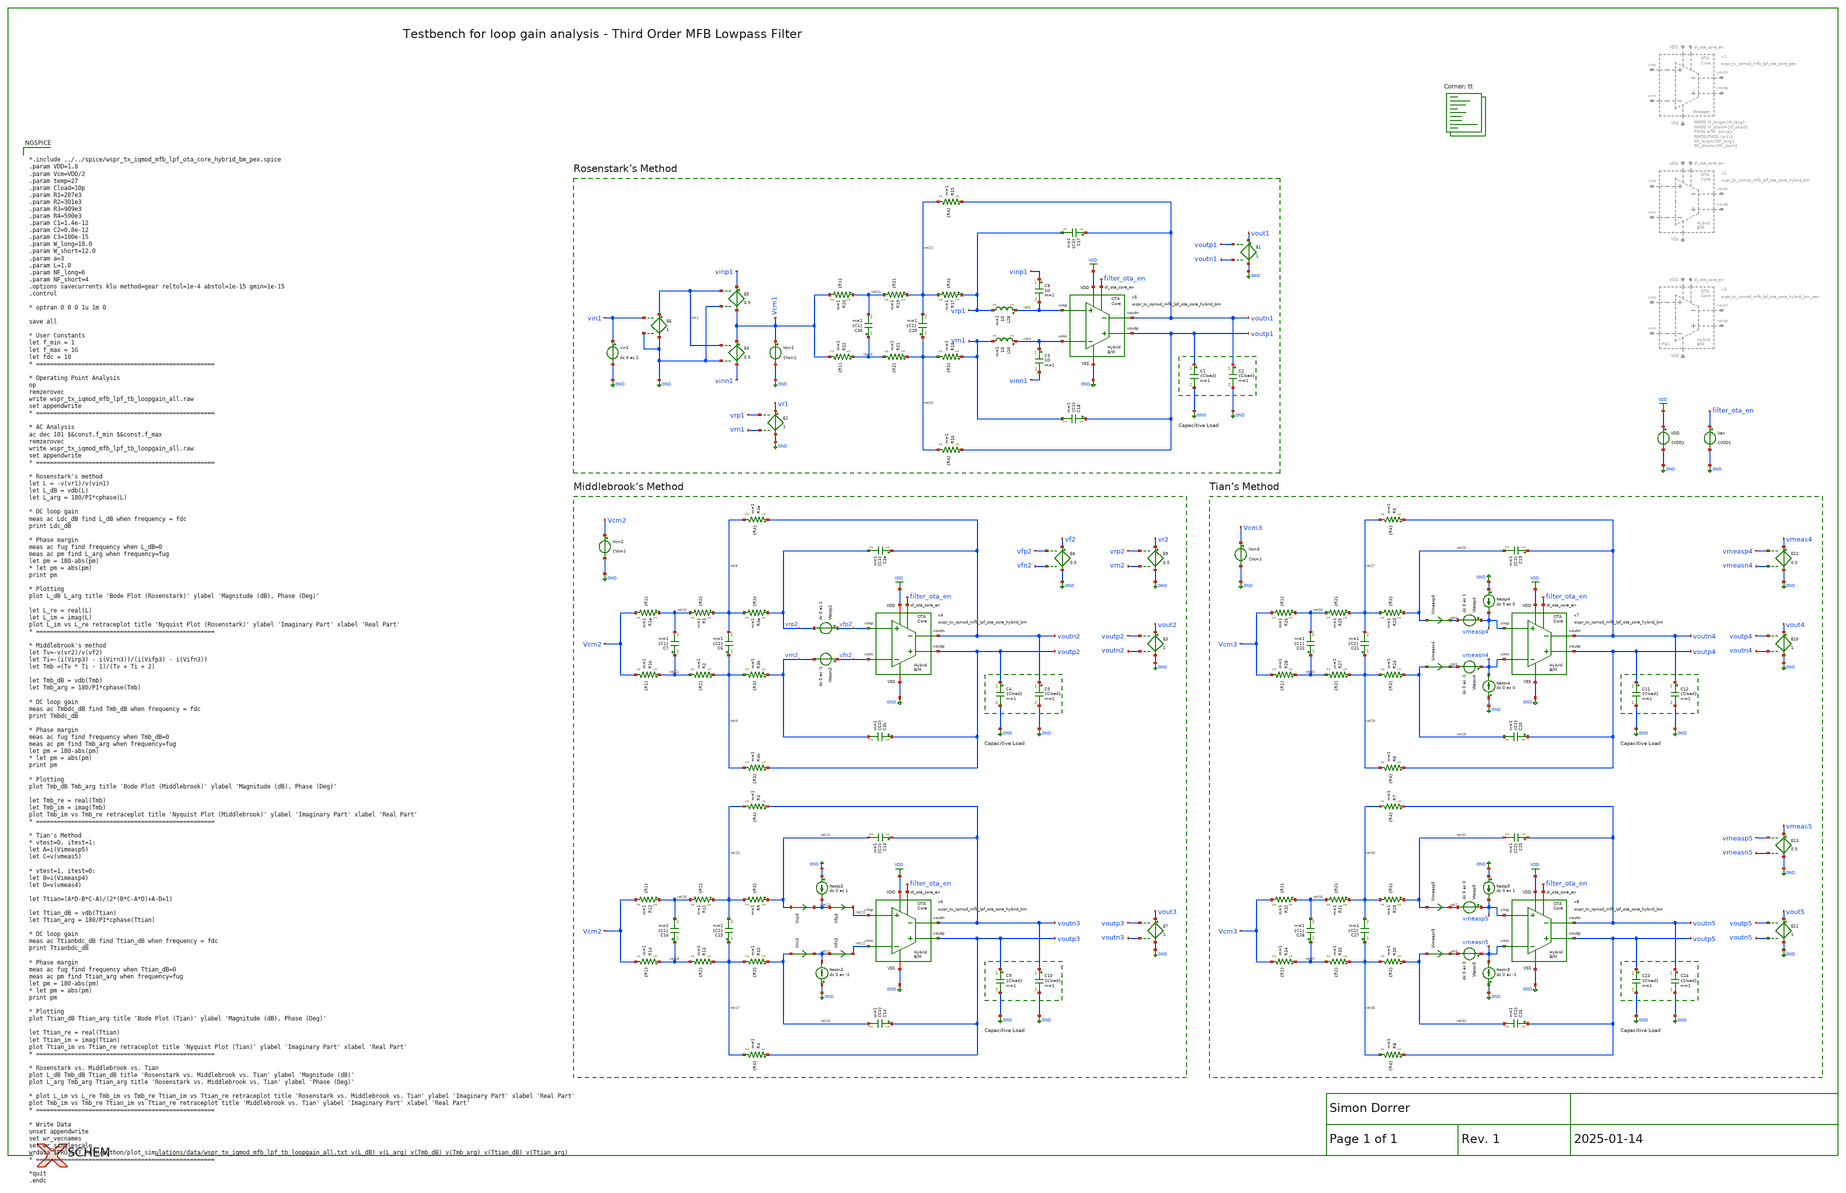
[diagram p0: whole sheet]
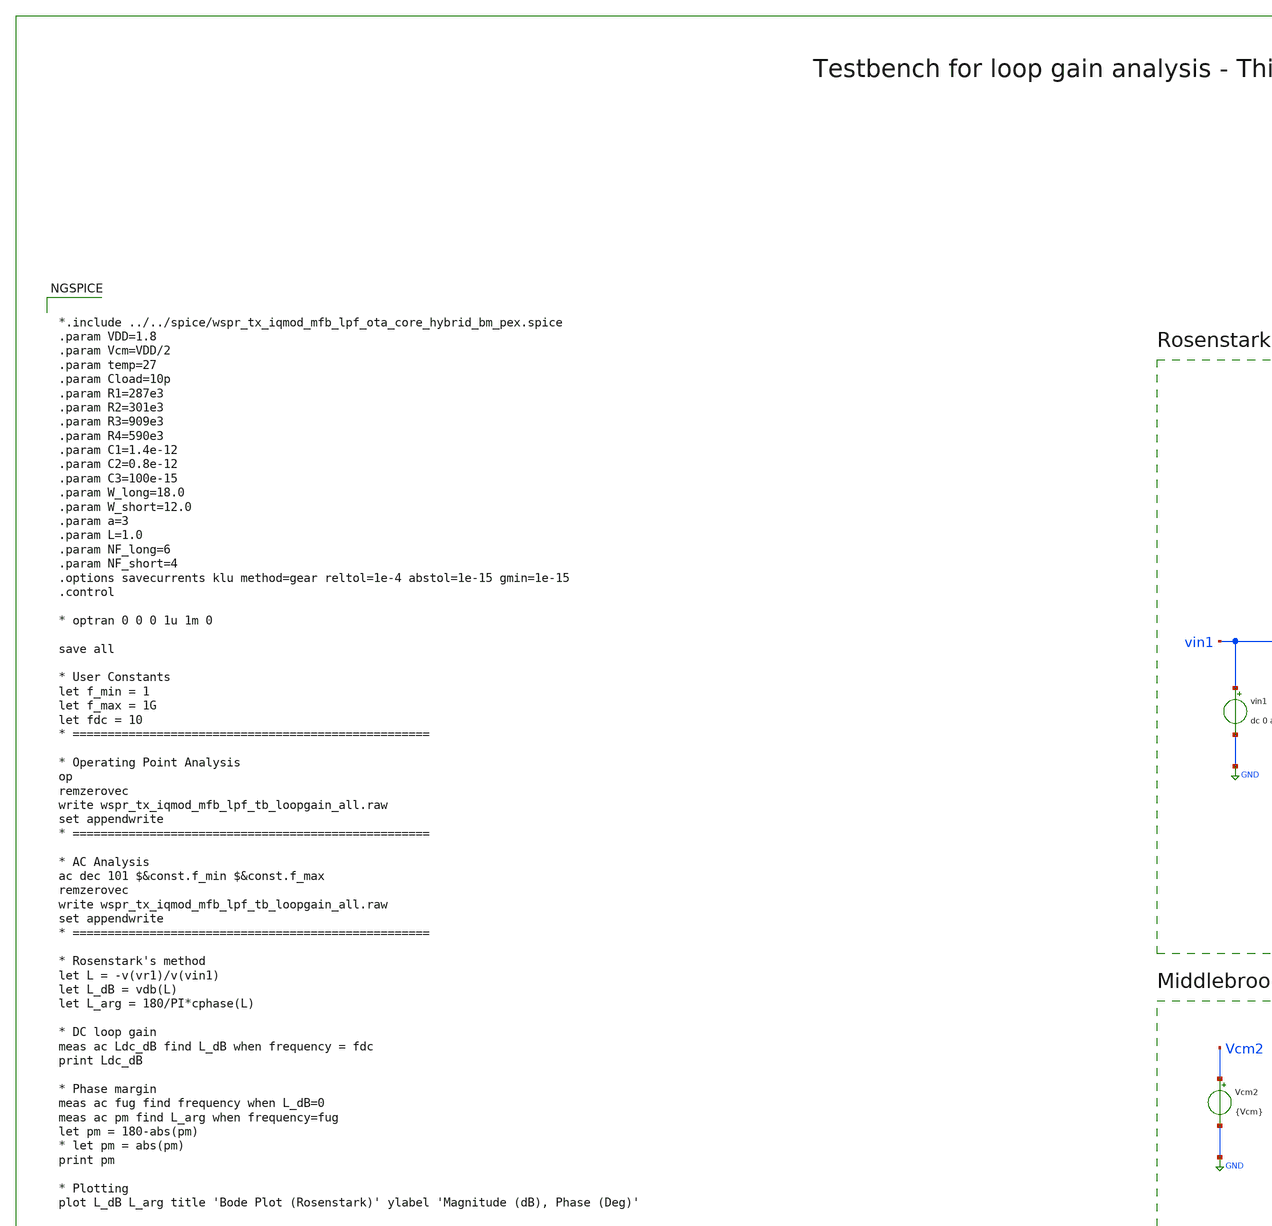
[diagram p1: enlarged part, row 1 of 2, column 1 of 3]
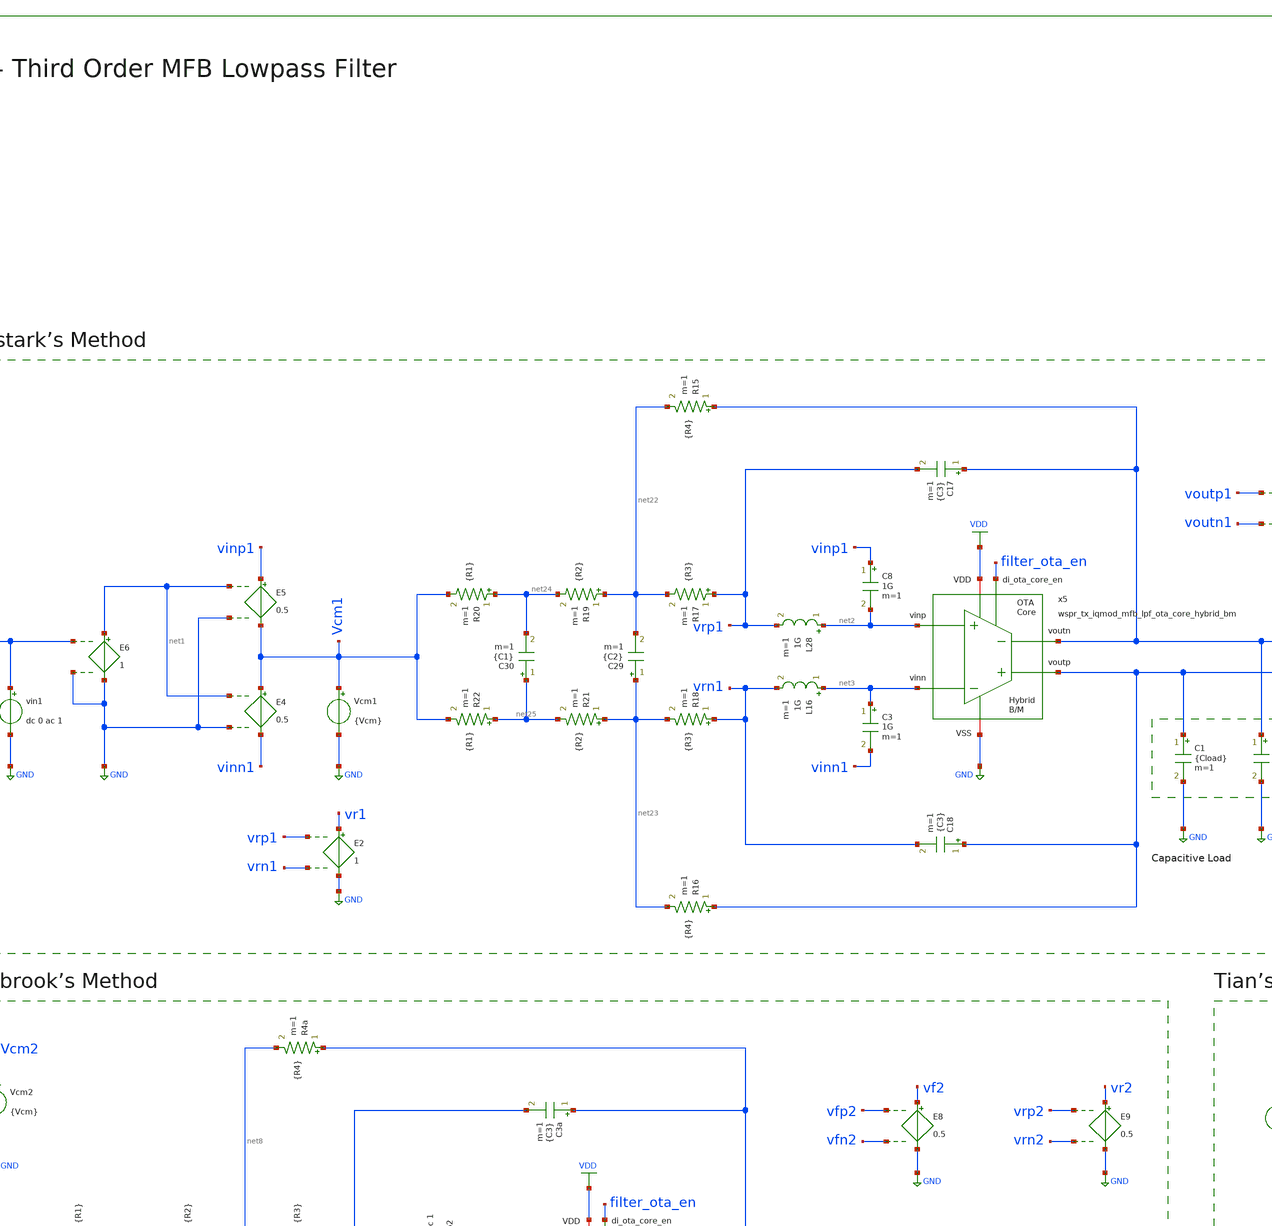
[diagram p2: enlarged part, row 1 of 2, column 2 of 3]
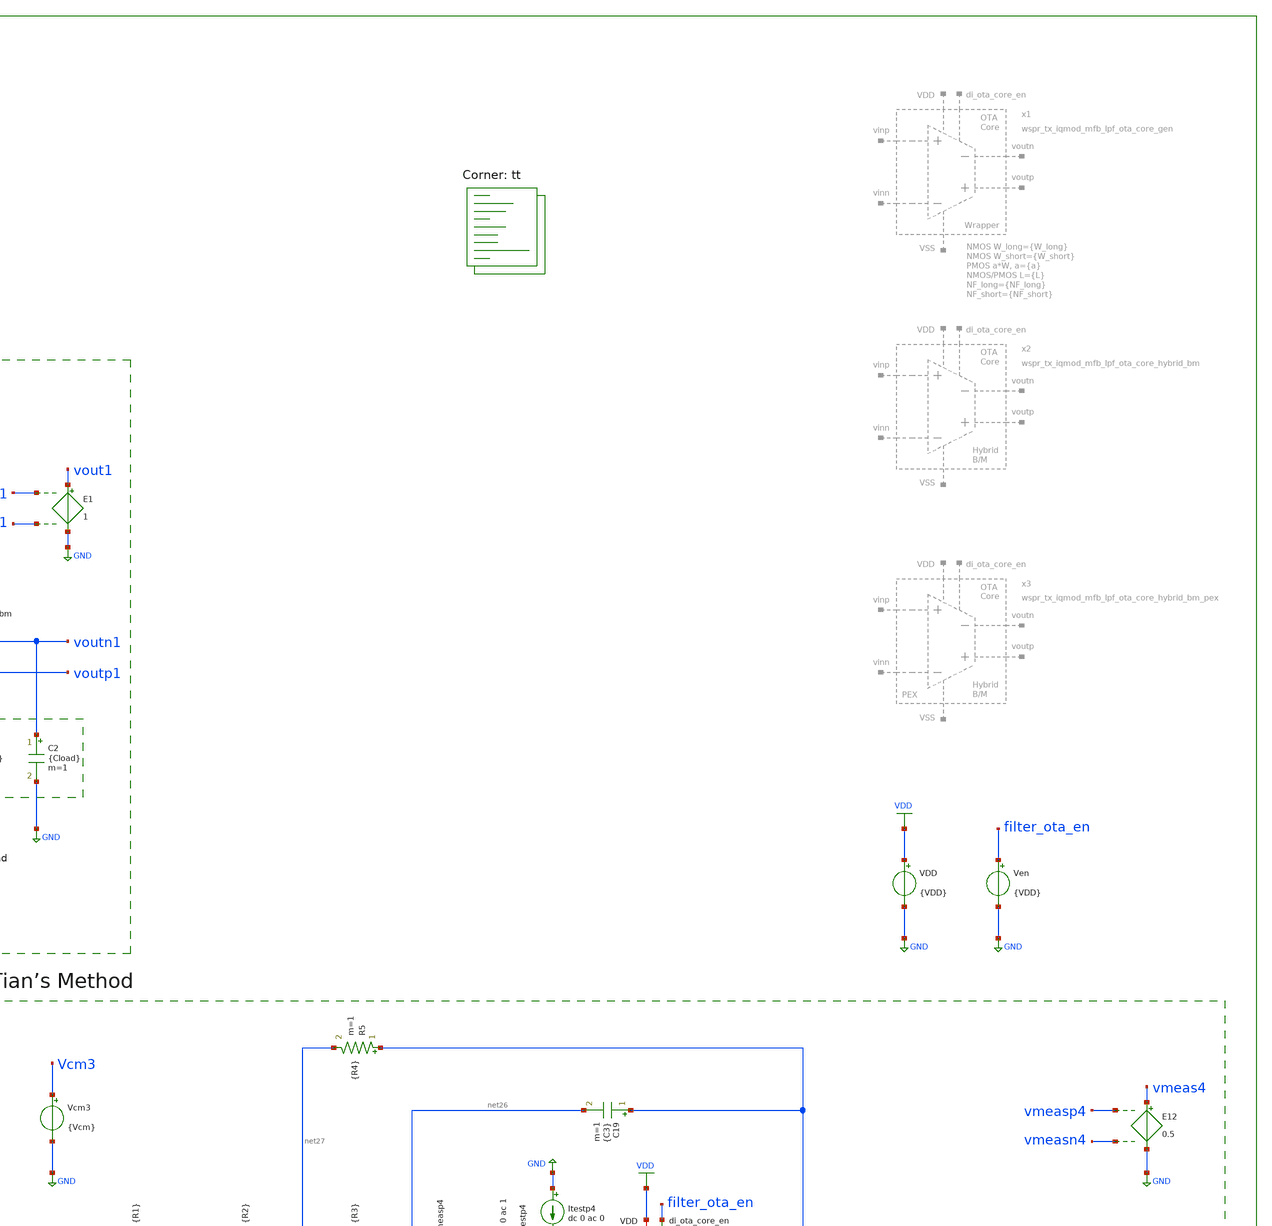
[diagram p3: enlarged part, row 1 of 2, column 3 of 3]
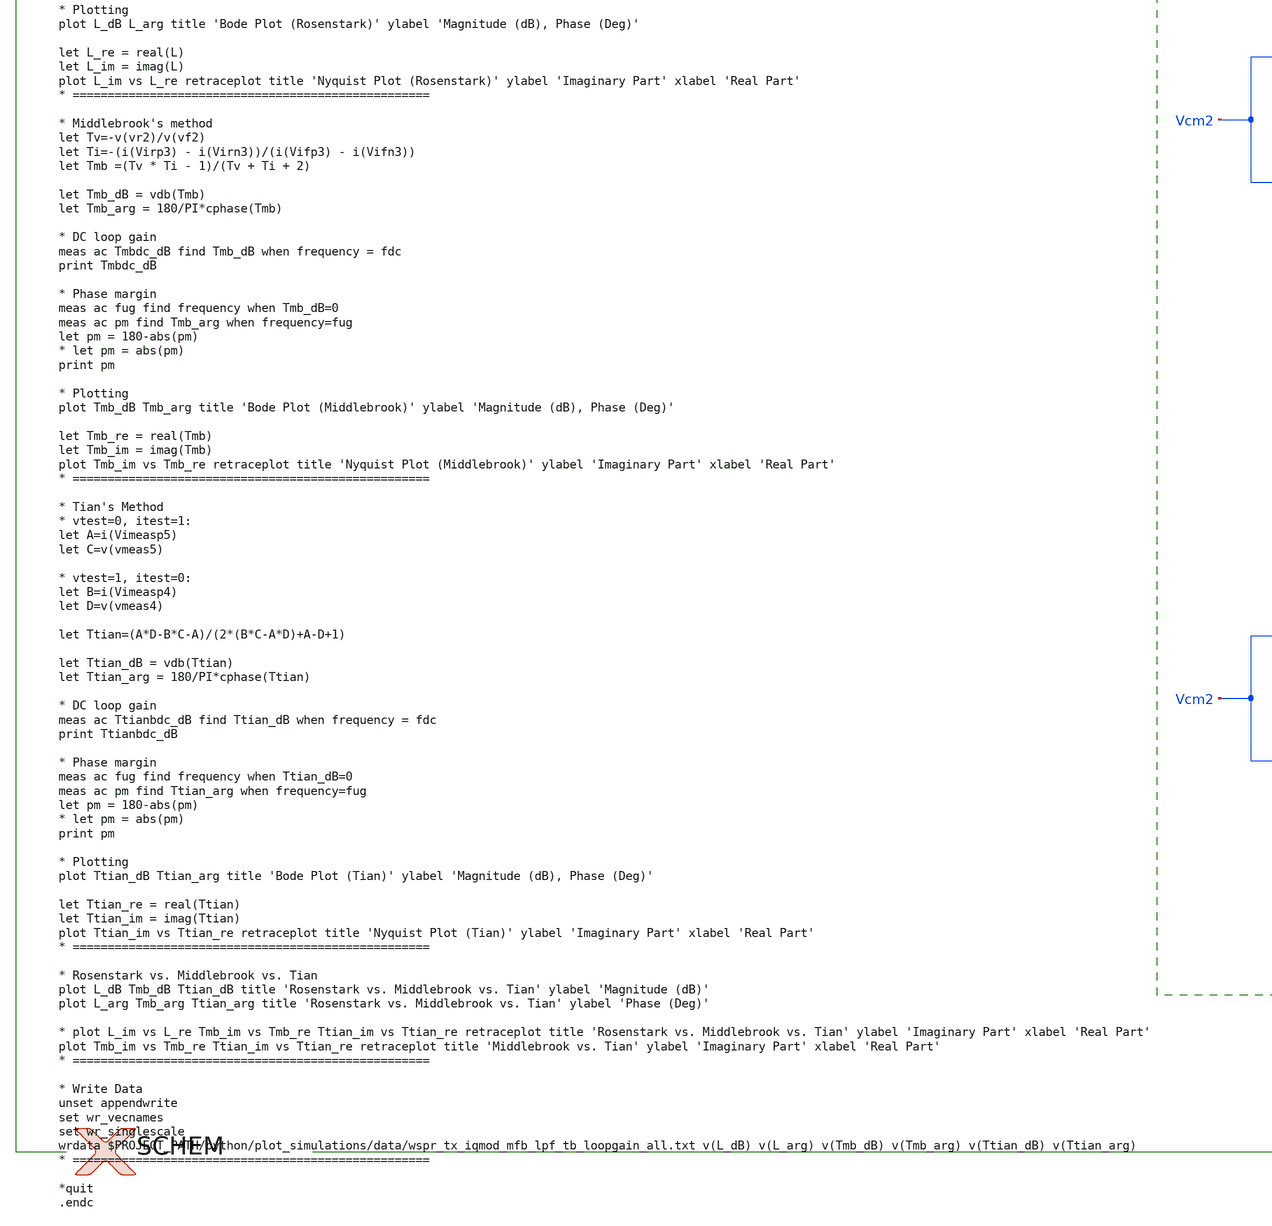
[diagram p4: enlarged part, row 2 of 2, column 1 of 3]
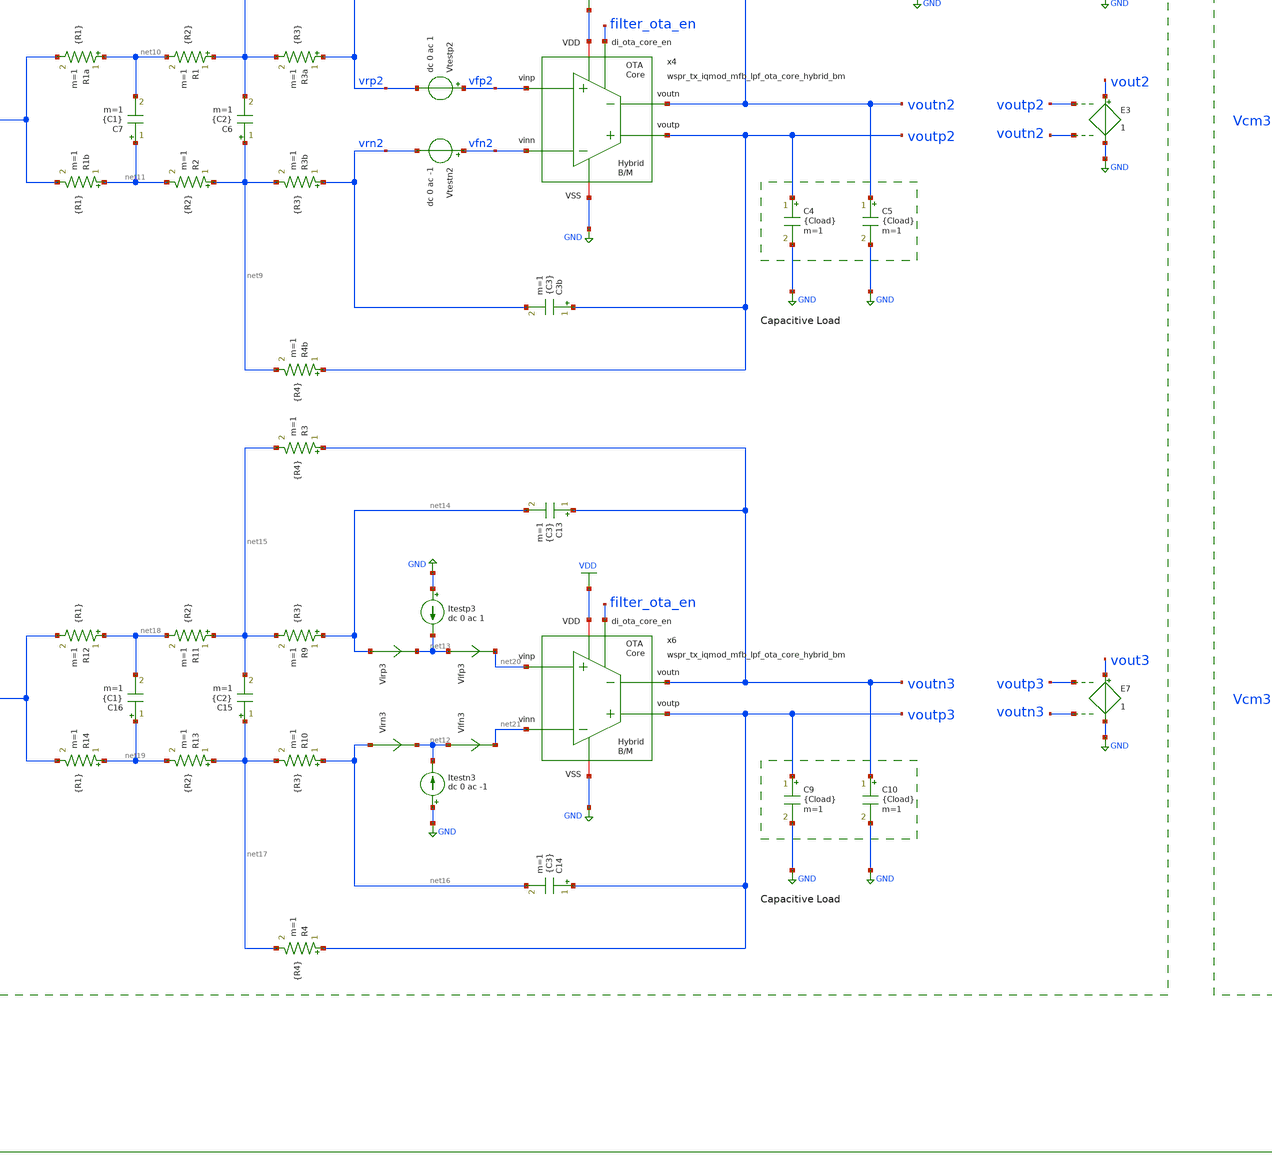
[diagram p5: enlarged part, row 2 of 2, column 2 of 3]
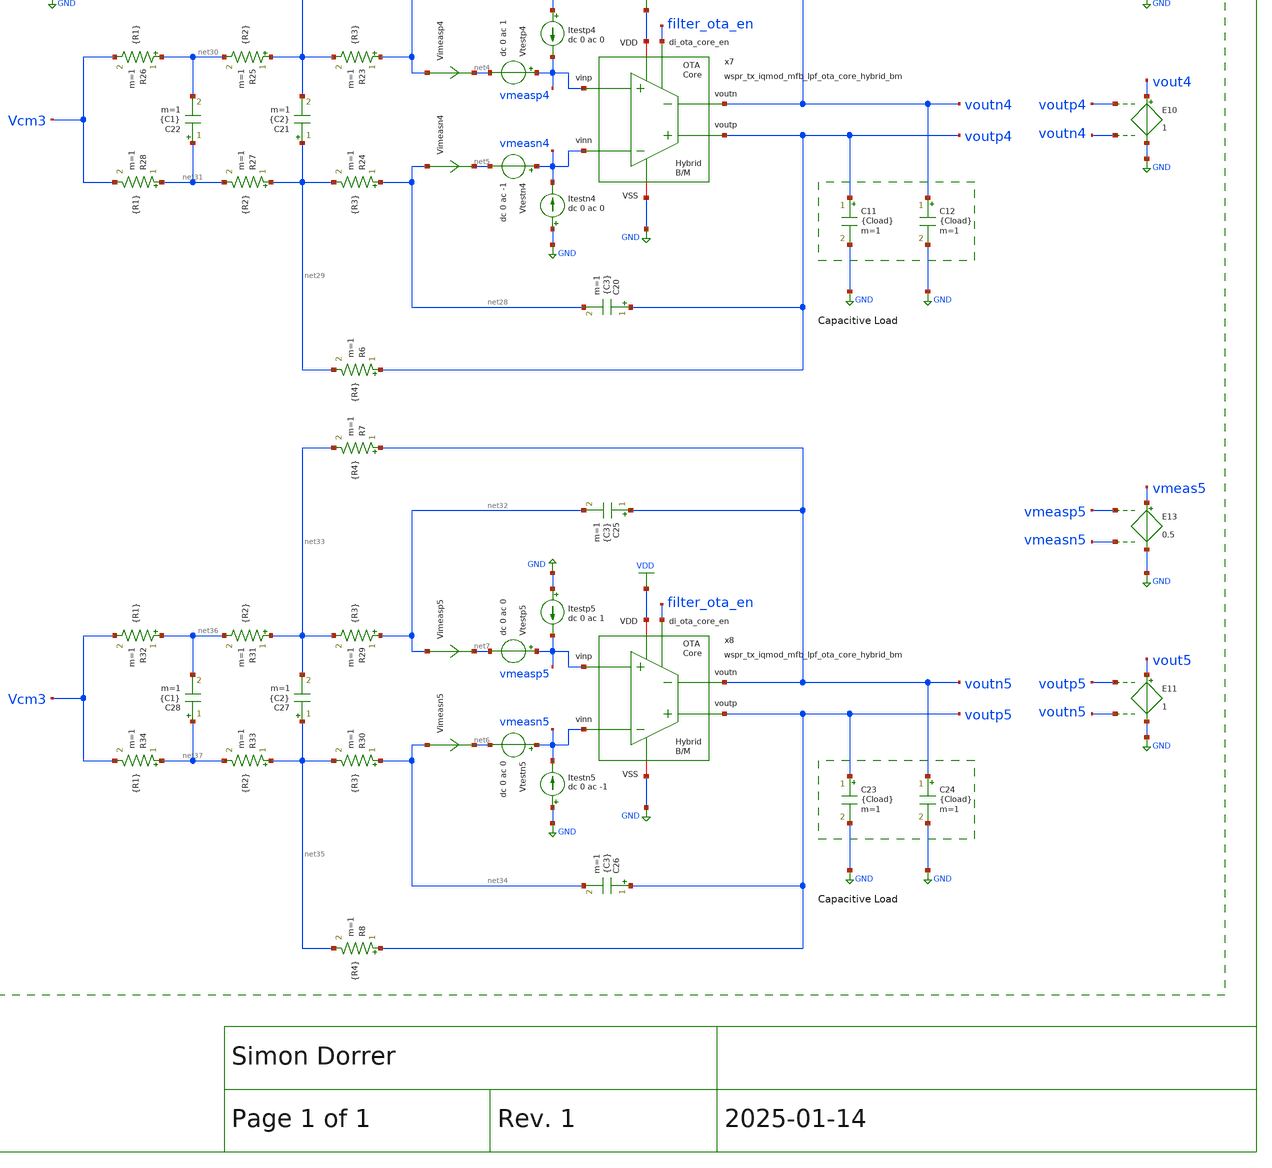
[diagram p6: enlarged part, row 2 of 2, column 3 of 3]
** sch_path: sky130/macros/iqmod/testbenches/wspr_tx_iqmod_mfb_lpf_tb_loopgain_all.sch
**.subckt wspr_tx_iqmod_mfb_lpf_tb_loopgain_all
VDD VDD GND {VDD}
Vcm1 Vcm1 GND {Vcm}
E4 Vcm1 vinn1 net1 GND 0.5
E5 vinp1 Vcm1 net1 GND 0.5
E6 net1 GND vin1 GND 1
Ven filter_ota_en GND {VDD}
E1 vout1 GND voutp1 voutn1 1
vin1 vin1 GND dc 0 ac 1
C8 vinp1 net2 1G m=1
L28 net2 vrp1 1G m=1
L16 net3 vrn1 1G m=1
C3 net3 vinn1 1G m=1
E2 vr1 GND vrp1 vrn1 1
E10 vout4 GND voutp4 voutn4 1
E11 vout5 GND voutp5 voutn5 1
Vtestp4 vmeasp4 net4 dc 0 ac 1
Vimeasp4 net26 net4 0
.save i(vimeasp4)
Itestp4 GND vmeasp4 dc 0 ac 0
Vimeasn4 net28 net5 0
.save i(vimeasn4)
Vtestn4 vmeasn4 net5 dc 0 ac -1
Itestn4 GND vmeasn4 dc 0 ac 0
Vimeasn5 net34 net6 0
.save i(vimeasn5)
Vtestn5 vmeasn5 net6 dc 0 ac 0
Itestn5 GND vmeasn5 dc 0 ac -1
Vtestp5 vmeasp5 net7 dc 0 ac 0
Vimeasp5 net32 net7 0
.save i(vimeasp5)
Itestp5 GND vmeasp5 dc 0 ac 1
E12 vmeas4 GND vmeasp4 vmeasn4 0.5
E13 vmeas5 GND vmeasp5 vmeasn5 0.5
Vcm2 Vcm2 GND {Vcm}
Vcm3 Vcm3 GND {Vcm}
C4 voutp2 GND {Cload} m=1
C5 voutn2 GND {Cload} m=1
E3 vout2 GND voutp2 voutn2 1
R4a voutn2 net8 {R4} m=1
R4b voutp2 net9 {R4} m=1
C3a voutn2 vrp2 {C3} m=1
C3b voutp2 vrn2 {C3} m=1
C6 net9 net8 {C2} m=1
E8 vf2 GND vfp2 vfn2 0.5
E9 vr2 GND vrp2 vrn2 0.5
Vtestp2 vfp2 vrp2 dc 0 ac 1
Vtestn2 vfn2 vrn2 dc 0 ac -1
R3a vrp2 net8 {R3} m=1
R3b vrn2 net9 {R3} m=1
R1 net8 net10 {R2} m=1
R1a net10 Vcm2 {R1} m=1
R2 net9 net11 {R2} m=1
R1b net11 Vcm2 {R1} m=1
C7 net11 net10 {C1} m=1
E7 vout3 GND voutp3 voutn3 1
Virp3 net14 net13 0
.save i(virp3)
Vifp3 net13 net20 0
.save i(vifp3)
Itestn3 GND net12 dc 0 ac -1
Virn3 net16 net12 0
.save i(virn3)
Vifn3 net12 net21 0
.save i(vifn3)
Itestp3 GND net13 dc 0 ac 1
C9 voutp3 GND {Cload} m=1
C10 voutn3 GND {Cload} m=1
R3 voutn3 net15 {R4} m=1
R4 voutp3 net17 {R4} m=1
C13 voutn3 net14 {C3} m=1
C14 voutp3 net16 {C3} m=1
C15 net17 net15 {C2} m=1
R9 net14 net15 {R3} m=1
R10 net16 net17 {R3} m=1
R11 net15 net18 {R2} m=1
R12 net18 Vcm2 {R1} m=1
R13 net17 net19 {R2} m=1
R14 net19 Vcm2 {R1} m=1
C16 net19 net18 {C1} m=1
C1 voutp1 GND {Cload} m=1
C2 voutn1 GND {Cload} m=1
R15 voutn1 net22 {R4} m=1
R16 voutp1 net23 {R4} m=1
C17 voutn1 vrp1 {C3} m=1
C18 voutp1 vrn1 {C3} m=1
C29 net23 net22 {C2} m=1
R17 vrp1 net22 {R3} m=1
R18 vrn1 net23 {R3} m=1
R19 net22 net24 {R2} m=1
R20 net24 Vcm1 {R1} m=1
R21 net23 net25 {R2} m=1
R22 net25 Vcm1 {R1} m=1
C30 net25 net24 {C1} m=1
C11 voutp4 GND {Cload} m=1
C12 voutn4 GND {Cload} m=1
R5 voutn4 net27 {R4} m=1
R6 voutp4 net29 {R4} m=1
C19 voutn4 net26 {C3} m=1
C20 voutp4 net28 {C3} m=1
C21 net29 net27 {C2} m=1
R23 net26 net27 {R3} m=1
R24 net28 net29 {R3} m=1
R25 net27 net30 {R2} m=1
R26 net30 Vcm3 {R1} m=1
R27 net29 net31 {R2} m=1
R28 net31 Vcm3 {R1} m=1
C22 net31 net30 {C1} m=1
C23 voutp5 GND {Cload} m=1
C24 voutn5 GND {Cload} m=1
R7 voutn5 net33 {R4} m=1
R8 voutp5 net35 {R4} m=1
C25 voutn5 net32 {C3} m=1
C26 voutp5 net34 {C3} m=1
C27 net35 net33 {C2} m=1
R29 net32 net33 {R3} m=1
R30 net34 net35 {R3} m=1
R31 net33 net36 {R2} m=1
R32 net36 Vcm3 {R1} m=1
R33 net35 net37 {R2} m=1
R34 net37 Vcm3 {R1} m=1
C28 net37 net36 {C1} m=1
x5 filter_ota_en voutp1 voutn1 net3 net2 VDD GND wspr_tx_iqmod_mfb_lpf_ota_core_hybrid_bm
x4 filter_ota_en voutp2 voutn2 vfn2 vfp2 VDD GND wspr_tx_iqmod_mfb_lpf_ota_core_hybrid_bm
x6 filter_ota_en voutp3 voutn3 net21 net20 VDD GND wspr_tx_iqmod_mfb_lpf_ota_core_hybrid_bm
x7 filter_ota_en voutp4 voutn4 vmeasn4 vmeasp4 VDD GND wspr_tx_iqmod_mfb_lpf_ota_core_hybrid_bm
x8 filter_ota_en voutp5 voutn5 vmeasn5 vmeasp5 VDD GND wspr_tx_iqmod_mfb_lpf_ota_core_hybrid_bm
**** begin user architecture code


*.include ../../spice/wspr_tx_iqmod_mfb_lpf_ota_core_hybrid_bm_pex.spice
.param VDD=1.8
.param Vcm=VDD/2
.param temp=27
.param Cload=10p
.param R1=287e3
.param R2=301e3
.param R3=909e3
.param R4=590e3
.param C1=1.4e-12
.param C2=0.8e-12
.param C3=100e-15
.param W_long=18.0
.param W_short=12.0
.param a=3
.param L=1.0
.param NF_long=6
.param NF_short=4
.options savecurrents klu method=gear reltol=1e-4 abstol=1e-15 gmin=1e-15
.control

* optran 0 0 0 1u 1m 0

save all

* User Constants
let f_min = 1
let f_max = 1G
let fdc = 10
* ===================================================

* Operating Point Analysis
op
remzerovec
write wspr_tx_iqmod_mfb_lpf_tb_loopgain_all.raw
set appendwrite
* ===================================================

* AC Analysis
ac dec 101 $&const.f_min $&const.f_max
remzerovec
write wspr_tx_iqmod_mfb_lpf_tb_loopgain_all.raw
set appendwrite
* ===================================================

* Rosenstark's method
let L = -v(vr1)/v(vin1)
let L_dB = vdb(L)
let L_arg = 180/PI*cphase(L)

* DC loop gain
meas ac Ldc_dB find L_dB when frequency = fdc
print Ldc_dB

* Phase margin
meas ac fug find frequency when L_dB=0
meas ac pm find L_arg when frequency=fug
let pm = 180-abs(pm)
* let pm = abs(pm)
print pm

* Plotting
plot L_dB L_arg title 'Bode Plot (Rosenstark)' ylabel 'Magnitude (dB), Phase (Deg)'

let L_re = real(L)
let L_im = imag(L)
plot L_im vs L_re retraceplot title 'Nyquist Plot (Rosenstark)' ylabel 'Imaginary Part' xlabel 'Real
+ Part'
* ===================================================

* Middlebrook's method
let Tv=-v(vr2)/v(vf2)
let Ti=-(i(Virp3) - i(Virn3))/(i(Vifp3) - i(Vifn3))
let Tmb =(Tv * Ti - 1)/(Tv + Ti + 2)

let Tmb_dB = vdb(Tmb)
let Tmb_arg = 180/PI*cphase(Tmb)

* DC loop gain
meas ac Tmbdc_dB find Tmb_dB when frequency = fdc
print Tmbdc_dB

* Phase margin
meas ac fug find frequency when Tmb_dB=0
meas ac pm find Tmb_arg when frequency=fug
let pm = 180-abs(pm)
* let pm = abs(pm)
print pm

* Plotting
plot Tmb_dB Tmb_arg title 'Bode Plot (Middlebrook)' ylabel 'Magnitude (dB), Phase (Deg)'

let Tmb_re = real(Tmb)
let Tmb_im = imag(Tmb)
plot Tmb_im vs Tmb_re retraceplot title 'Nyquist Plot (Middlebrook)' ylabel 'Imaginary Part' xlabel 'Real Part'
* ===================================================

* Tian's Method
* vtest=0, itest=1:
let A=i(Vimeasp5)
let C=v(vmeas5)

* vtest=1, itest=0:
let B=i(Vimeasp4)
let D=v(vmeas4)

let Ttian=(A*D-B*C-A)/(2*(B*C-A*D)+A-D+1)

let Ttian_dB = vdb(Ttian)
let Ttian_arg = 180/PI*cphase(Ttian)

* DC loop gain
meas ac Ttianbdc_dB find Ttian_dB when frequency = fdc
print Ttianbdc_dB

* Phase margin
meas ac fug find frequency when Ttian_dB=0
meas ac pm find Ttian_arg when frequency=fug
let pm = 180-abs(pm)
* let pm = abs(pm)
print pm

* Plotting
plot Ttian_dB Ttian_arg title 'Bode Plot (Tian)' ylabel 'Magnitude (dB), Phase (Deg)'

let Ttian_re = real(Ttian)
let Ttian_im = imag(Ttian)
plot Ttian_im vs Ttian_re retraceplot title 'Nyquist Plot (Tian)' ylabel 'Imaginary Part' xlabel 'Real
+ Part'
* ===================================================

* Rosenstark vs. Middlebrook vs. Tian
plot L_dB Tmb_dB Ttian_dB title 'Rosenstark vs. Middlebrook vs. Tian' ylabel 'Magnitude (dB)'
plot L_arg Tmb_arg Ttian_arg title 'Rosenstark vs. Middlebrook vs. Tian' ylabel 'Phase (Deg)'

* plot L_im vs L_re Tmb_im vs Tmb_re Ttian_im vs Ttian_re retraceplot title 'Rosenstark vs. Middlebrook
*+ vs. Tian' ylabel 'Imaginary Part' xlabel 'Real Part'
plot Tmb_im vs Tmb_re Ttian_im vs Ttian_re retraceplot title 'Middlebrook vs. Tian' ylabel 'Imaginary
+ Part' xlabel 'Real Part'
* ===================================================

* Write Data
unset appendwrite
set wr_vecnames
set wr_singlescale
wrdata $PROJECT_PATH/python/plot_simulations/data/wspr_tx_iqmod_mfb_lpf_tb_loopgain_all.txt v(L_dB) v(L_arg) v(Tmb_dB) v(Tmb_arg) v(Ttian_dB) v(Ttian_arg)
* ===================================================

*quit
.endc


.lib $::SKYWATER_MODELS/sky130.lib.spice tt
**** end user architecture code
**.ends
.GLOBAL GND
.GLOBAL VDD
.end
